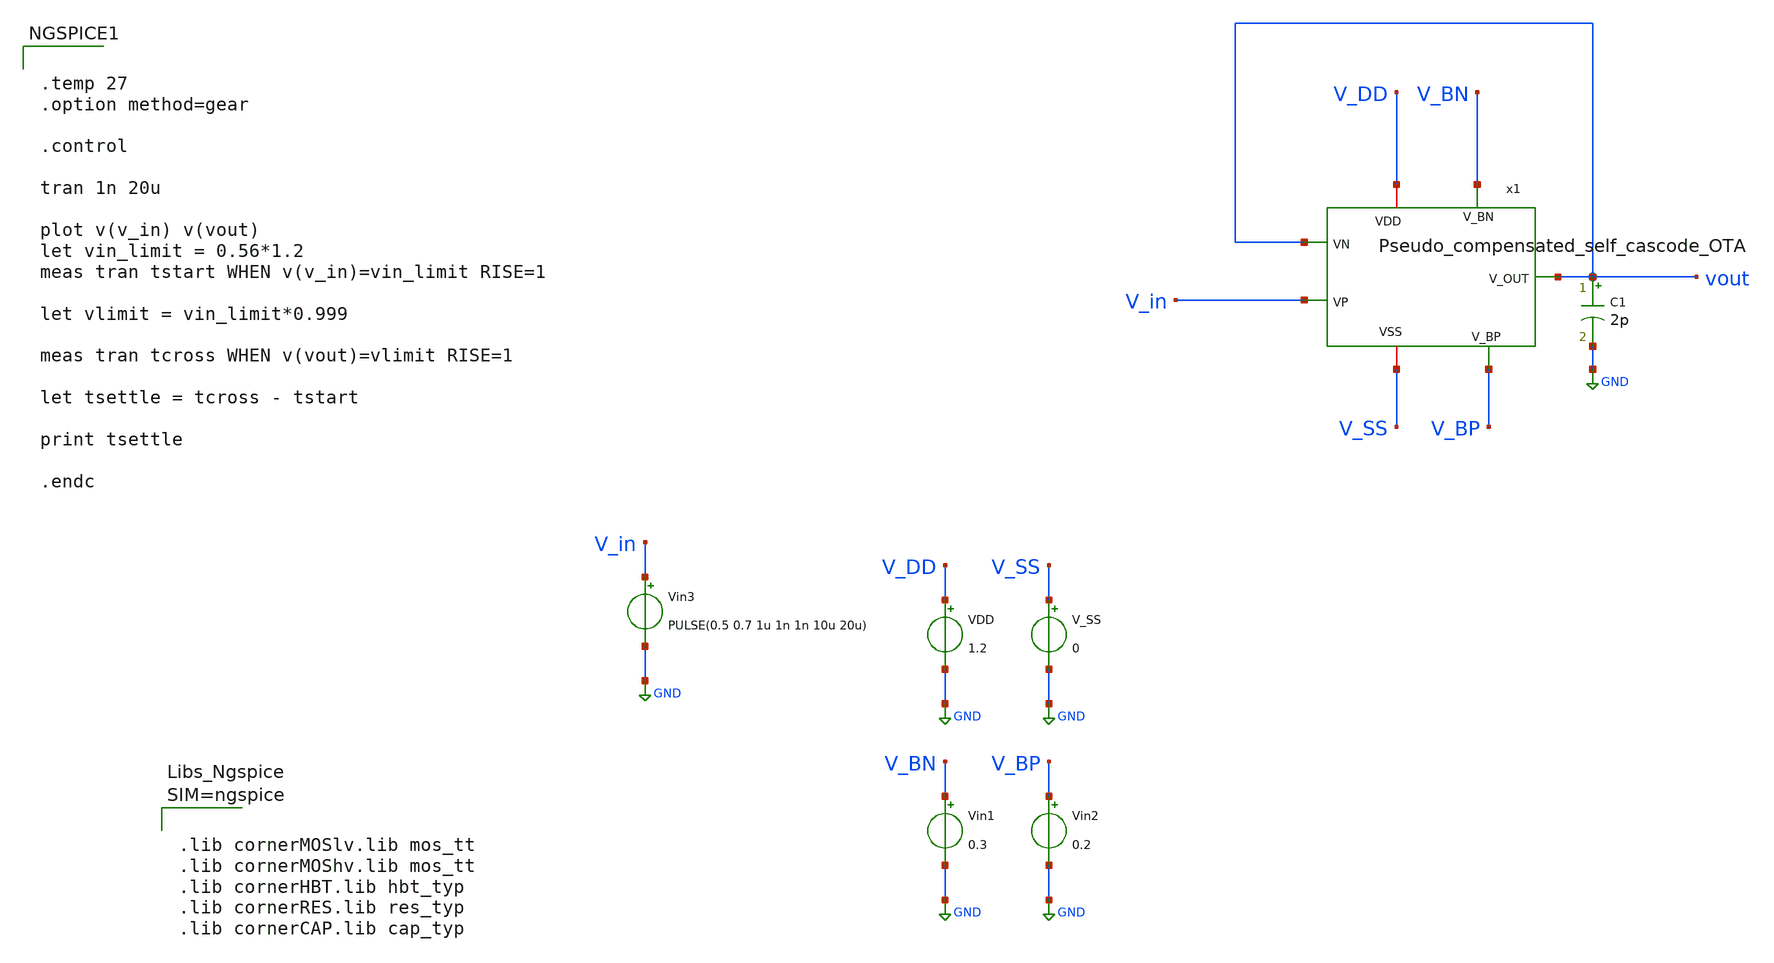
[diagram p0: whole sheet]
** sch_path: xschem/OTA_tb_tran.sch
**.subckt OTA_tb_tran
VDD V_DD GND 1.2
V_SS V_SS GND 0
Vin1 V_BN GND 0.3
Vin2 V_BP GND 0.2
x1 vout V_in V_BN V_BP vout V_DD V_SS Pseudo_compensated_self_cascode_OTA
C1 vout GND 2p m=1
Vin3 V_in GND PULSE(0.5 0.7 1u 1n 1n 10u 20u)
**** begin user architecture code



.lib cornerMOSlv.lib mos_tt
.lib cornerMOShv.lib mos_tt
.lib cornerHBT.lib hbt_typ
.lib cornerRES.lib res_typ
.lib cornerCAP.lib cap_typ





.temp 27
.option method=gear

.control

tran 1n 20u

plot v(v_in) v(vout)
let vin_limit = 0.56*1.2
meas tran tstart WHEN v(v_in)=vin_limit RISE=1

let vlimit = vin_limit*0.999

meas tran tcross WHEN v(vout)=vlimit RISE=1

let tsettle = tcross - tstart

print tsettle

.endc


**** end user architecture code
**.ends

* expanding   symbol:  Pseudo_compensated_self_cascode_OTA.sym # of pins=7
** sym_path: xschem/Pseudo_compensated_self_cascode_OTA.sym
** sch_path: xschem/Pseudo_compensated_self_cascode_OTA.sch
.subckt Pseudo_compensated_self_cascode_OTA VN VP V_BN V_BP V_OUT VDD VSS
*.ipin VN
*.ipin VP
*.ipin V_BN
*.ipin V_BP
*.opin V_OUT
*.iopin VDD
*.iopin VSS
XM11 net1 VN net2 VSS sg13_lv_nmos w=70u l=0.8u ng=7 m=1 mm_ok=1
XM12 V_GS VN net1 V_BP sg13_lv_nmos w=38.5u l=0.3u ng=4 m=1 mm_ok=1
XM21 net4 VP net2 VSS sg13_lv_nmos w=70u l=0.8u ng=7 m=1 mm_ok=1
XM22 VB32 VP net4 V_BP sg13_lv_nmos w=38.5u l=0.3u ng=4 m=1 mm_ok=1
XM52 net2 V_BN net3 V_BN sg13_lv_nmos w=40u l=0.5u ng=4 m=1 mm_ok=1
XM51 net3 V_BN VSS VSS sg13_lv_nmos w=40u l=2.5u ng=4 m=1 mm_ok=1
XM32 V_GS V_GS VS32 VB32 sg13_lv_pmos w=48.5u l=1.24u ng=5 m=1 mm_ok=1
XM31 VS32 V_GS VDD VDD sg13_lv_pmos w=48.5u l=0.87u ng=5 m=1 mm_ok=1
XM42 VB32 V_GS VS42 V_GS sg13_lv_pmos w=48.5u l=1.24u ng=5 m=1 mm_ok=1
XM41 VS42 V_GS VDD VDD sg13_lv_pmos w=48.5u l=0.87u ng=5 m=1 mm_ok=1
XM61 net5 VB32 VDD VDD sg13_lv_pmos w=60u l=0.13u ng=6 m=1 mm_ok=1
XM62 V_OUT VB32 net5 V_BP sg13_lv_pmos w=60u l=0.13u ng=6 m=1 mm_ok=1
XM72 V_OUT V_BN net6 V_BN sg13_lv_nmos w=40u l=0.5u ng=10 m=1 mm_ok=1
XM71 net6 V_BN VSS VSS sg13_lv_nmos w=40u l=2.5u ng=4 m=1 mm_ok=1
XC3 VS42 V_OUT cap_cmim w=5.0e-6 l=5.0e-6 m=38 mm_ok=1
XC1 net4 V_OUT cap_cmim w=5.0e-6 l=5.0e-6 m=38 mm_ok=1
.ends

.GLOBAL GND
.end
